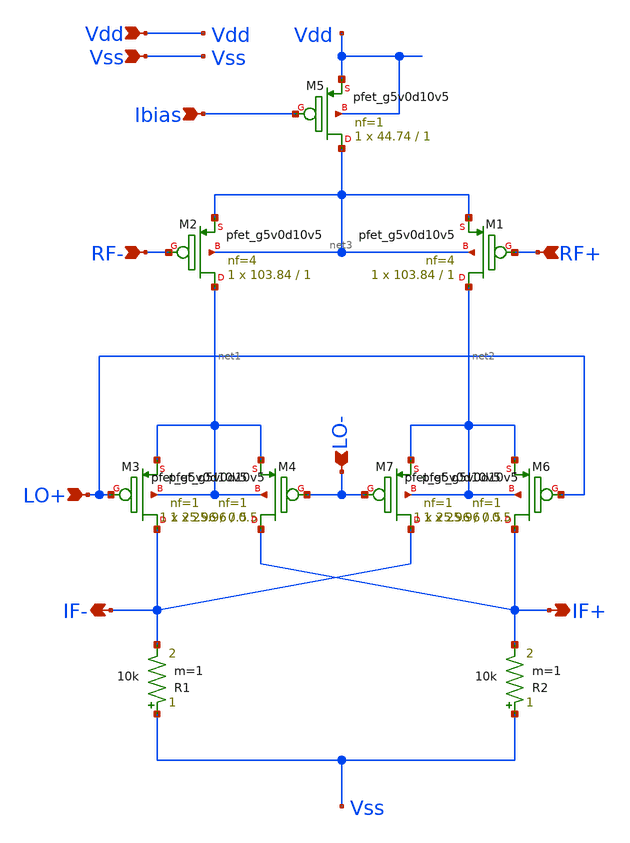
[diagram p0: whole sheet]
** sch_path: xschem/Gil_Mix.sch
**.subckt Gil_Mix RF- RF+ Vdd Vss Ibias LO- LO+ IF+ IF-
*.ipin RF-
*.ipin RF+
*.ipin Vdd
*.ipin Vss
*.ipin Ibias
*.ipin LO-
*.ipin LO+
*.opin IF+
*.opin IF-
XM1 net2 RF+ net3 net3 sky130_fd_pr__pfet_g5v0d10v5 L=1 W=103.84 nf=4 ad='int((4 + 1)/2) * 103.84 / 4 * 0.29'
+ as='int((4 + 2)/2) * 103.84 / 4 * 0.29' pd='2*int((4 + 1)/2) * (103.84 / 4 + 0.29)' ps='2*int((4 + 2)/2) * (103.84 / 4 + 0.29)'
+ nrd='0.29 / 103.84 ' nrs='0.29 / 103.84 ' sa=0 sb=0 sd=0 mult=1 m=1
XM2 net1 RF- net3 net3 sky130_fd_pr__pfet_g5v0d10v5 L=1 W=103.84 nf=4 ad='int((4 + 1)/2) * 103.84 / 4 * 0.29'
+ as='int((4 + 2)/2) * 103.84 / 4 * 0.29' pd='2*int((4 + 1)/2) * (103.84 / 4 + 0.29)' ps='2*int((4 + 2)/2) * (103.84 / 4 + 0.29)'
+ nrd='0.29 / 103.84 ' nrs='0.29 / 103.84 ' sa=0 sb=0 sd=0 mult=1 m=1
XM5 net3 Ibias Vdd Vdd sky130_fd_pr__pfet_g5v0d10v5 L=1 W=44.74 nf=1 ad='int((1 + 1)/2) * 44.74 / 1 * 0.29'
+ as='int((1 + 2)/2) * 44.74 / 1 * 0.29' pd='2*int((1 + 1)/2) * (44.74 / 1 + 0.29)' ps='2*int((1 + 2)/2) * (44.74 / 1 + 0.29)'
+ nrd='0.29 / 44.74 ' nrs='0.29 / 44.74 ' sa=0 sb=0 sd=0 mult=1 m=1
XM3 IF- LO+ net1 net1 sky130_fd_pr__pfet_g5v0d10v5 L=0.5 W=25.96 nf=1 ad='int((1 + 1)/2) * 25.96 / 1 * 0.29'
+ as='int((1 + 2)/2) * 25.96 / 1 * 0.29' pd='2*int((1 + 1)/2) * (25.96 / 1 + 0.29)' ps='2*int((1 + 2)/2) * (25.96 / 1 + 0.29)'
+ nrd='0.29 / 25.96 ' nrs='0.29 / 25.96 ' sa=0 sb=0 sd=0 mult=1 m=1
XM4 IF+ LO- net1 net1 sky130_fd_pr__pfet_g5v0d10v5 L=0.5 W=25.96 nf=1 ad='int((1 + 1)/2) * 25.96 / 1 * 0.29'
+ as='int((1 + 2)/2) * 25.96 / 1 * 0.29' pd='2*int((1 + 1)/2) * (25.96 / 1 + 0.29)' ps='2*int((1 + 2)/2) * (25.96 / 1 + 0.29)'
+ nrd='0.29 / 25.96 ' nrs='0.29 / 25.96 ' sa=0 sb=0 sd=0 mult=1 m=1
XM6 IF+ LO+ net2 net2 sky130_fd_pr__pfet_g5v0d10v5 L=0.5 W=25.96 nf=1 ad='int((1 + 1)/2) * 25.96 / 1 * 0.29'
+ as='int((1 + 2)/2) * 25.96 / 1 * 0.29' pd='2*int((1 + 1)/2) * (25.96 / 1 + 0.29)' ps='2*int((1 + 2)/2) * (25.96 / 1 + 0.29)'
+ nrd='0.29 / 25.96 ' nrs='0.29 / 25.96 ' sa=0 sb=0 sd=0 mult=1 m=1
XM7 IF- LO- net2 net2 sky130_fd_pr__pfet_g5v0d10v5 L=0.5 W=25.96 nf=1 ad='int((1 + 1)/2) * 25.96 / 1 * 0.29'
+ as='int((1 + 2)/2) * 25.96 / 1 * 0.29' pd='2*int((1 + 1)/2) * (25.96 / 1 + 0.29)' ps='2*int((1 + 2)/2) * (25.96 / 1 + 0.29)'
+ nrd='0.29 / 25.96 ' nrs='0.29 / 25.96 ' sa=0 sb=0 sd=0 mult=1 m=1
R1 Vss IF- 10k m=1
R2 Vss IF+ 10k m=1
**.ends
.end
